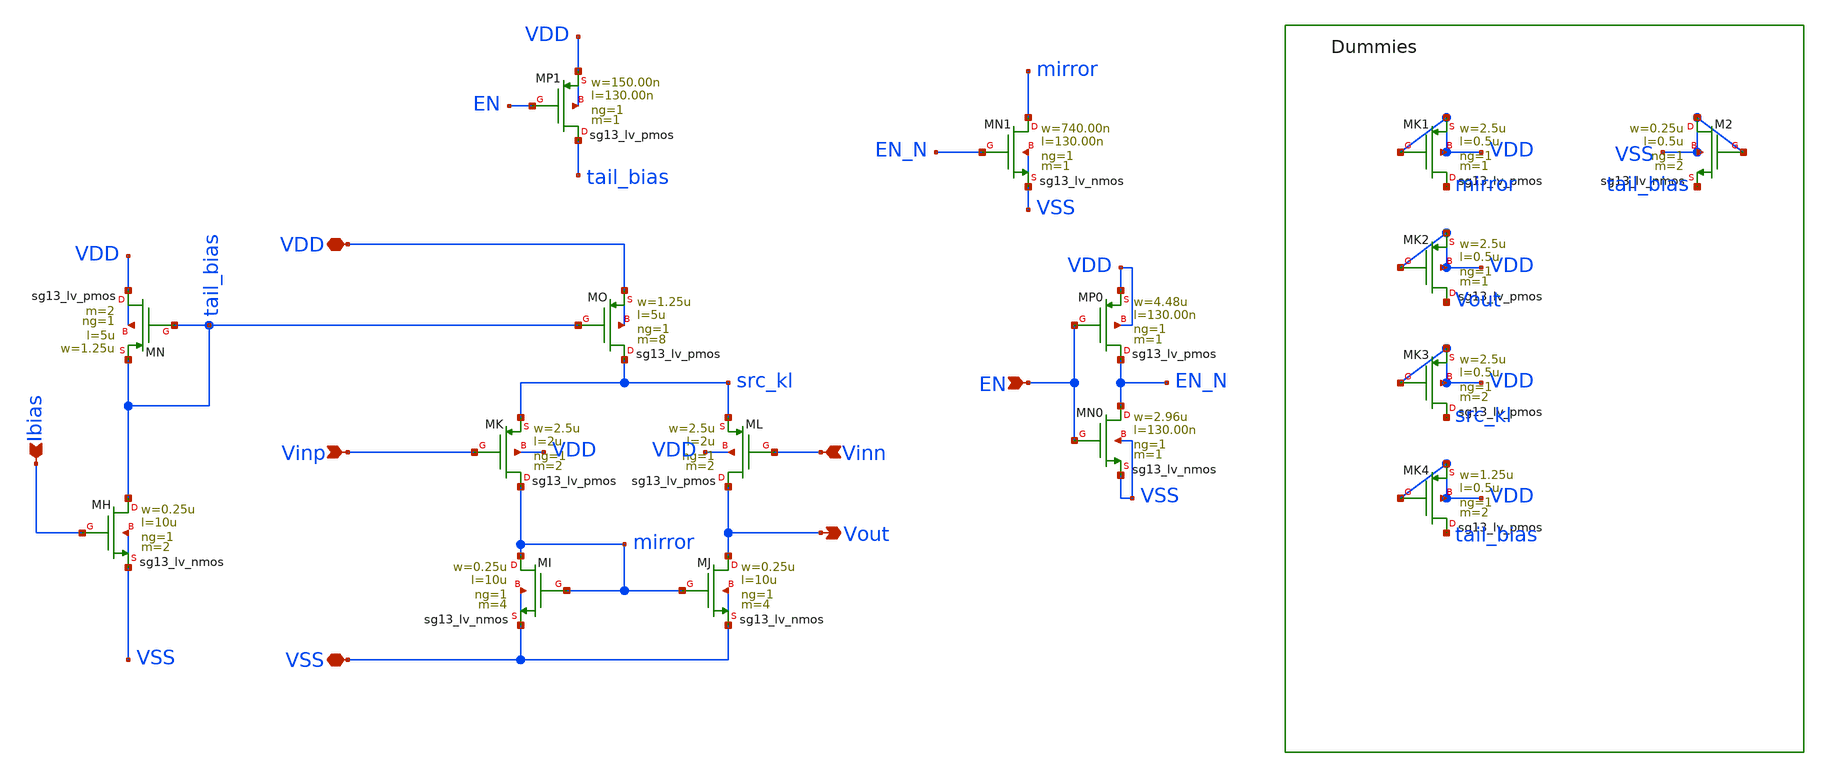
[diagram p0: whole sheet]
** sch_path: schema/ota_cmfb_fbota/ota_cmfb_fbota.sch
**.subckt ota_cmfb_fbota Vout VDD VSS Vinp Ibias Vinn EN
*.opin Vout
*.iopin VDD
*.iopin VSS
*.ipin Vinp
*.ipin Ibias
*.ipin Vinn
*.ipin EN
XMJ Vout mirror VSS VSS sg13_lv_nmos w=0.25u l=10u ng=1 m=4 mm_ok=1
XML Vout Vinn src_kl VDD sg13_lv_pmos w=2.5u l=2u ng=1 m=2 mm_ok=1
XMI mirror mirror VSS VSS sg13_lv_nmos w=0.25u l=10u ng=1 m=4 mm_ok=1
XMK mirror Vinp src_kl VDD sg13_lv_pmos w=2.5u l=2u ng=1 m=2 mm_ok=1
XMO src_kl tail_bias VDD VDD sg13_lv_pmos w=1.25u l=5u ng=1 m=8 mm_ok=1
XMN VDD tail_bias tail_bias VDD sg13_lv_pmos w=1.25u l=5u ng=1 m=2 mm_ok=1
XMH tail_bias Ibias VSS VSS sg13_lv_nmos w=0.25u l=10u ng=1 m=2 mm_ok=1
XMN1 mirror EN_N VSS VSS sg13_lv_nmos w=740.00n l=130.00n ng=1 m=1 mm_ok=1
XM2 VSS VSS tail_bias VSS sg13_lv_nmos w=0.25u l=0.5u ng=1 m=2 mm_ok=1
XMK1 mirror VDD VDD VDD sg13_lv_pmos w=2.5u l=0.5u ng=1 m=1 mm_ok=1
XMK2 Vout VDD VDD VDD sg13_lv_pmos w=2.5u l=0.5u ng=1 m=1 mm_ok=1
XMK3 src_kl VDD VDD VDD sg13_lv_pmos w=2.5u l=0.5u ng=1 m=2 mm_ok=1
XMK4 tail_bias VDD VDD VDD sg13_lv_pmos w=1.25u l=0.5u ng=1 m=2 mm_ok=1
XMN0 EN_N EN VSS VSS sg13_lv_nmos w=2.96u l=130.00n ng=1 m=1 mm_ok=1
XMP0 EN_N EN VDD VDD sg13_lv_pmos w=4.48u l=130.00n ng=1 m=1 mm_ok=1
XMP1 tail_bias EN VDD VDD sg13_lv_pmos w=150.00n l=130.00n ng=1 m=1 mm_ok=1
**.ends
.end
